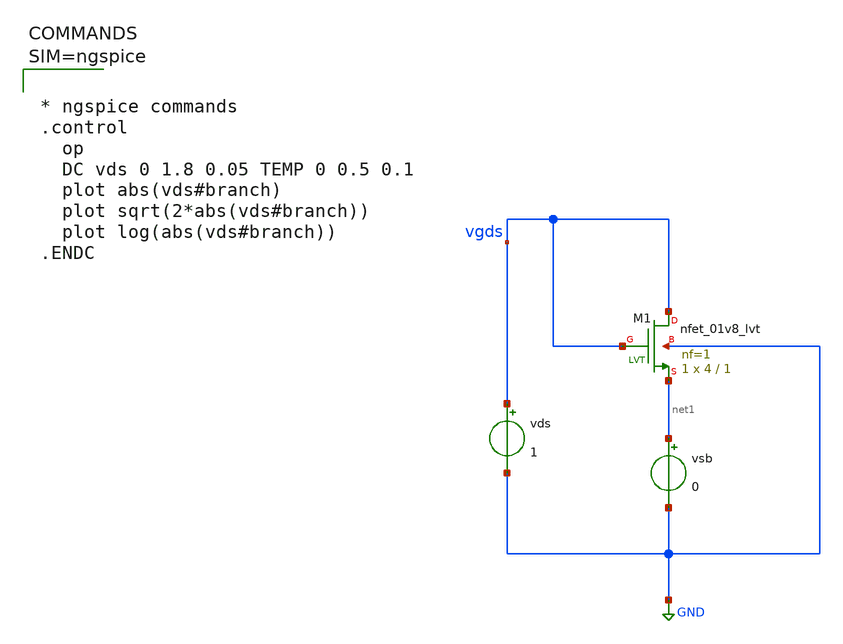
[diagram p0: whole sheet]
** sch_path: xschem/param.sch
**.subckt param
XM1 vgds vgds net1 GND sky130_fd_pr__nfet_01v8_lvt L=1 W=4 nf=1 ad='int((1 + 1)/2) * 4 / 1 * 0.29' as='int((1 + 2)/2) * 4 / 1 * 0.29'
+ pd='2*int((1 + 1)/2) * (4 / 1 + 0.29)' ps='2*int((1 + 2)/2) * (4 / 1 + 0.29)' nrd='0.29 / 4 ' nrs='0.29 / 4 '
+ sa=0 sb=0 sd=0 mult=1 m=1
vds vgds GND 1
vsb net1 GND 0
**** begin user architecture code

** opencircuitdesign pdks install
.lib $::SKYWATER_MODELS/sky130.lib.spice tt




* ngspice commands
.control
  op
  DC vds 0 1.8 0.05 TEMP 0 0.5 0.1
  plot abs(vds#branch)
  plot sqrt(2*abs(vds#branch))
  plot log(abs(vds#branch))
.ENDC



**** end user architecture code
**.ends
.GLOBAL GND
.end
